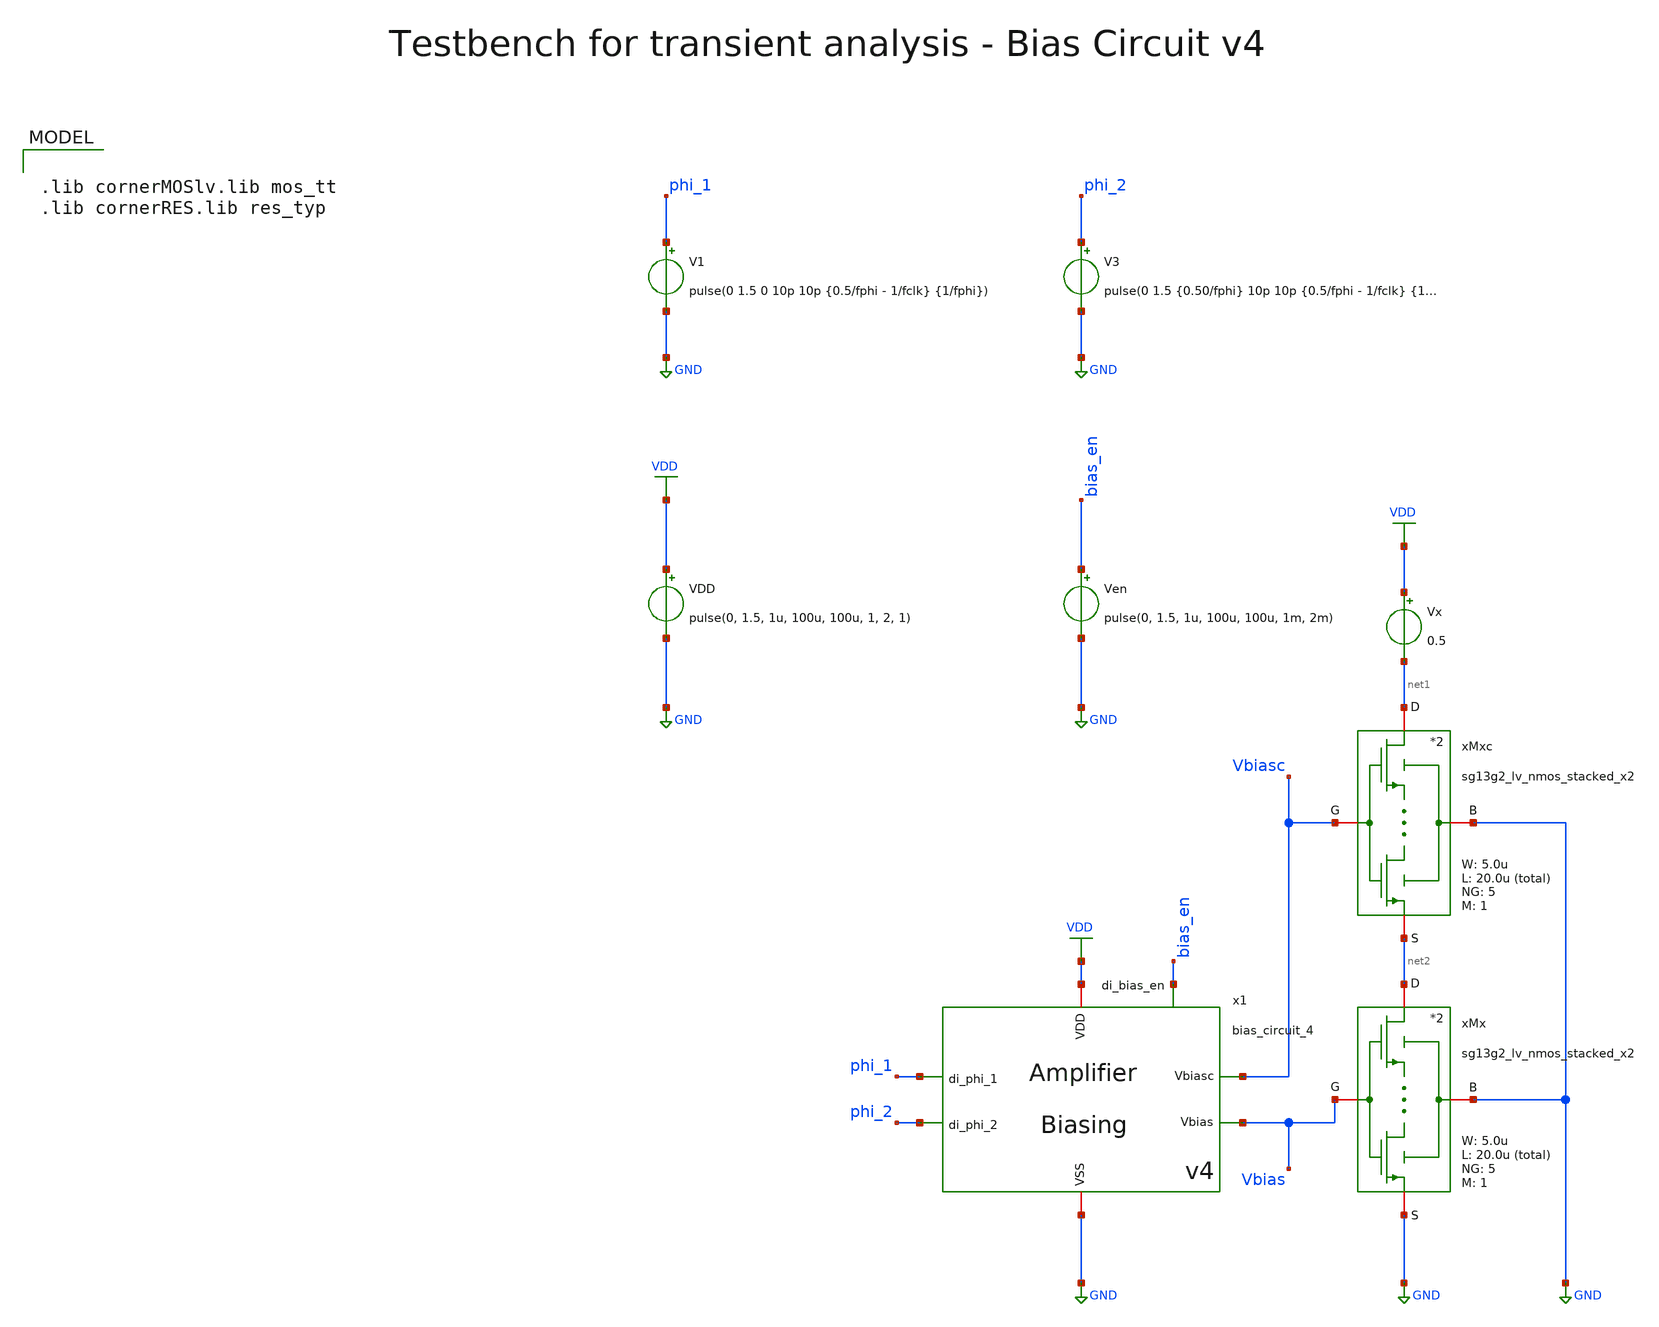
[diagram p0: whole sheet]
** sch_path: SG13G2_ATBS-ADC-main/xschem/bio_amplifier/amplifier_core/bias_circuit/bias_circuit_4/testbenches/bias_circuit_4_tb_startup_tran.sch
**.subckt bias_circuit_4_tb_startup_tran
x1 phi_2 phi_1 VDD GND Vbiasc Vbias bias_en bias_circuit_4
V1 phi_1 GND pulse(0 1.5 0 10p 10p {0.5/fphi - 1/fclk} {1/fphi})
V3 phi_2 GND pulse(0 1.5 {0.50/fphi} 10p 10p {0.5/fphi - 1/fclk} {1/fphi})
Vx VDD net1 0.5
xMx net2 Vbias GND GND sg13g2_lv_nmos_stacked_x2 W_N=5.0u L_N=20.0u NG_N=5 M_N=1
xMxc net1 Vbiasc GND net2 sg13g2_lv_nmos_stacked_x2 W_N=5.0u L_N=20.0u NG_N=5 M_N=1
Ven bias_en GND pulse(0, 1.5, 1u, 100u, 100u, 1m, 2m)
VDD VDD GND pulse(0, 1.5, 1u, 100u, 100u, 1, 2, 1)
**** begin user architecture code

.lib cornerMOSlv.lib mos_tt
.lib cornerRES.lib res_typ



.param temp=27
.param fclk=8000000
.param fphi=62500
.csparam fclk=fclk
.options reltol=1e-2 abstol=1e-15 gmin=1e-15
.control

* save all
save v(VDD) v(Vbias) v(Vbiasc) v(bias_en) v(x1.Vsu) v(x1.Vres) i(v.x1.viout) i(Vx) v(phi_1) v(phi_2)

* User constants
let tstep = 1/fclk

* Operating Point Analysis
op
remzerovec
write bias_circuit_4_tb_startup_tran.raw
set appendwrite

* Transient Analysis
tran $&tstep 1m
write bias_circuit_4_tb_startup_tran.raw

* Plotting
plot v(VDD) v(Vbias) v(Vbiasc) v(bias_en) v(x1.Vsu) v(x1.Vres)
plot i(v.x1.viout)
plot i(Vx)

* Measurement
let Iout_nominal = 10e-9
let Iout_99_percent = 0.99 * Iout_nominal
print Iout_99_percent
meas tran tsettle WHEN i(v.x1.viout)=Iout_99_percent from=10e-6 to=1e-3

* Write Data
set wr_vecnames
set wr_singlescale
let Vsu=x1.Vsu
let Vres=x1.Vres
wrdata
+ /foss/designs/SG13G2_ATBS-ADC-main/python/plot_simulations/data/bias_circuit_4_tb_startup_tran.txt v(VDD) v(Vbias) v(Vbiasc) v(bias_en) v(Vsu) v(Vres)

*quit
.endc

**** end user architecture code
**.ends
.GLOBAL GND
.GLOBAL VDD
.end
